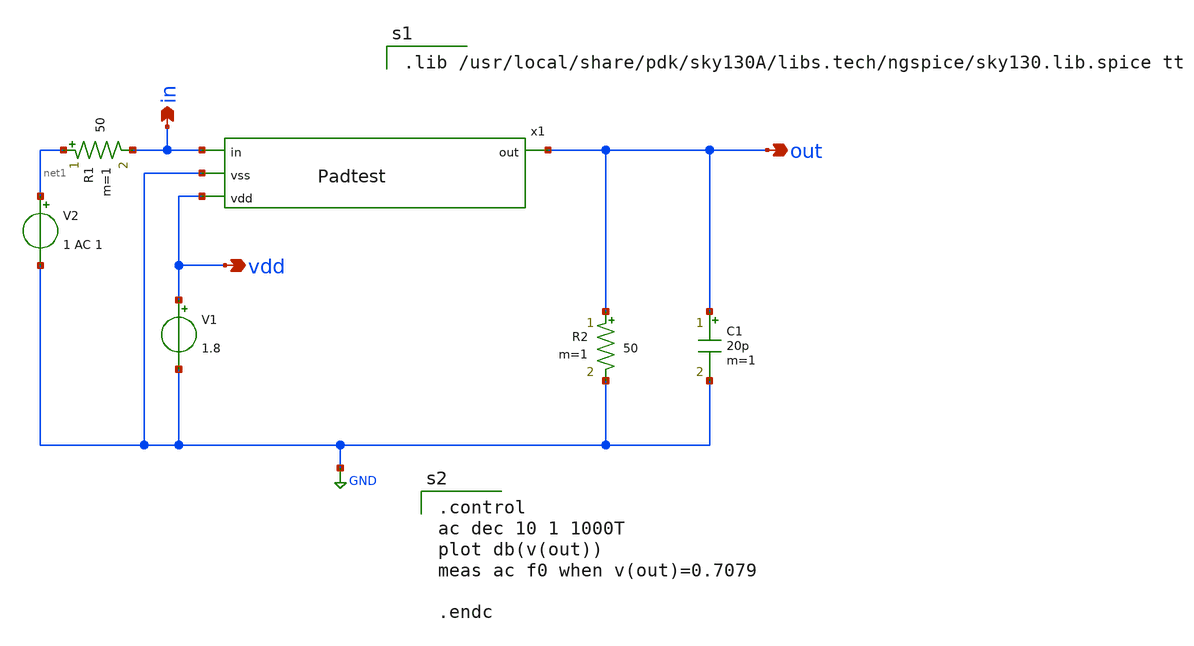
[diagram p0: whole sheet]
** sch_path: IO-cells/xschem/BW_tb.sch
**.subckt BW_tb out in vdd
*.opin out
*.opin in
*.opin vdd
V2 net1 GND 1 AC 1
x1 in GND vdd out Padtest
V1 vdd GND 1.8
C1 out GND 20p m=1
R2 out GND 50 m=1
R1 net1 in 50 m=1
**** begin user architecture code

.lib /usr/local/share/pdk/sky130A/libs.tech/ngspice/sky130.lib.spice tt


.control
ac dec 10 1 1000T
plot db(v(out))
meas ac f0 when v(out)=0.7079

.endc

**** end user architecture code
**.ends

* expanding   symbol:  Padtest.sym # of pins=4
** sym_path: IO-cells/xschem/Padtest.sym
** sch_path: IO-cells/xschem/Padtest.sch
.subckt Padtest in vss vdd out
*.ipin in
*.opin out
*.ipin vss
*.ipin vdd
R1 out in sky130_fd_pr__res_generic_m5 W=200 L=2 m=1
x1 vdd out vss SigPad
.ends


* expanding   symbol:  SigPad.sym # of pins=3
** sym_path: IO-cells/xschem/SigPad.sym
** sch_path: IO-cells/xschem/SigPad.sch
.subckt SigPad vdd in vss
*.ipin in
*.ipin vdd
*.ipin vss
XD1 in vdd sky130_fd_pr__diode_pd2nw_05v5 area=1000e12 pj=4e6
XD2 vss in sky130_fd_pr__diode_pw2nd_05v5 area=1000e12 pj=4e6
.ends

.GLOBAL GND
.end
